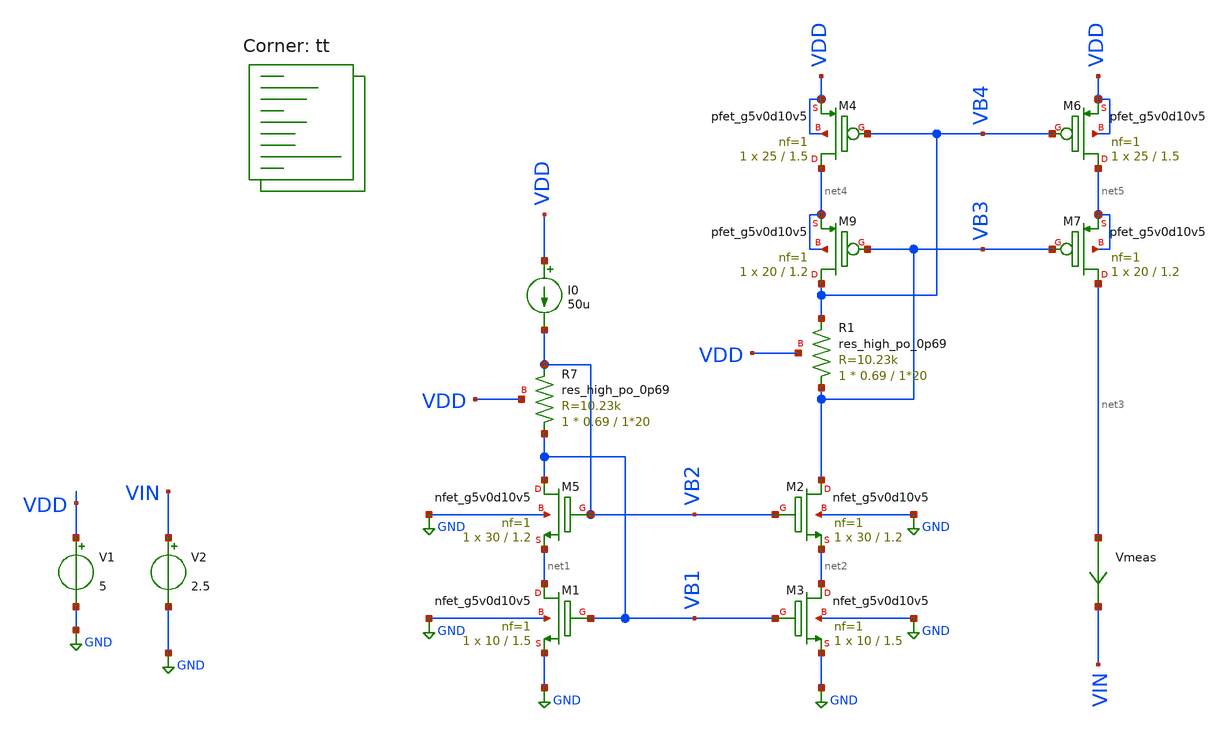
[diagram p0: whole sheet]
** sch_path: folded_cascode_amplifier_upgraded/1_stage/circ_test.sch
**.subckt circ_test
V1 VDD GND 5
V2 VIN GND 2.5
XM5 VB1 VB2 net1 GND sky130_fd_pr__nfet_g5v0d10v5 L=1.2 W=30 nf=1 ad='int((1 + 1)/2) * 30 / 1 * 0.29'
+ as='int((1 + 2)/2) * 30 / 1 * 0.29' pd='2*int((1 + 1)/2) * (30 / 1 + 0.29)' ps='2*int((1 + 2)/2) * (30 / 1 + 0.29)'
+ nrd='0.29 / 30 ' nrs='0.29 / 30 ' sa=0 sb=0 sd=0 mult=1 m=1
XM1 net1 VB1 GND GND sky130_fd_pr__nfet_g5v0d10v5 L=1.5 W=10 nf=1 ad='int((1 + 1)/2) * 10 / 1 * 0.29'
+ as='int((1 + 2)/2) * 10 / 1 * 0.29' pd='2*int((1 + 1)/2) * (10 / 1 + 0.29)' ps='2*int((1 + 2)/2) * (10 / 1 + 0.29)'
+ nrd='0.29 / 10 ' nrs='0.29 / 10 ' sa=0 sb=0 sd=0 mult=1 m=1
XR7 VB1 VB2 VDD sky130_fd_pr__res_high_po_0p69 L=1*20 mult=1 m=1
I0 VDD VB2 50u
XM2 VB3 VB2 net2 GND sky130_fd_pr__nfet_g5v0d10v5 L=1.2 W=30 nf=1 ad='int((1 + 1)/2) * 30 / 1 * 0.29'
+ as='int((1 + 2)/2) * 30 / 1 * 0.29' pd='2*int((1 + 1)/2) * (30 / 1 + 0.29)' ps='2*int((1 + 2)/2) * (30 / 1 + 0.29)'
+ nrd='0.29 / 30 ' nrs='0.29 / 30 ' sa=0 sb=0 sd=0 mult=1 m=1
XM3 net2 VB1 GND GND sky130_fd_pr__nfet_g5v0d10v5 L=1.5 W=10 nf=1 ad='int((1 + 1)/2) * 10 / 1 * 0.29'
+ as='int((1 + 2)/2) * 10 / 1 * 0.29' pd='2*int((1 + 1)/2) * (10 / 1 + 0.29)' ps='2*int((1 + 2)/2) * (10 / 1 + 0.29)'
+ nrd='0.29 / 10 ' nrs='0.29 / 10 ' sa=0 sb=0 sd=0 mult=1 m=1
Vmeas net3 VIN 0
.save i(vmeas)
XR1 VB3 VB4 VDD sky130_fd_pr__res_high_po_0p69 L=1*20 mult=1 m=1
XM9 VB4 VB3 net4 net4 sky130_fd_pr__pfet_g5v0d10v5 L=1.2 W=20 nf=1 ad='int((1 + 1)/2) * 20 / 1 * 0.29'
+ as='int((1 + 2)/2) * 20 / 1 * 0.29' pd='2*int((1 + 1)/2) * (20 / 1 + 0.29)' ps='2*int((1 + 2)/2) * (20 / 1 + 0.29)'
+ nrd='0.29 / 20 ' nrs='0.29 / 20 ' sa=0 sb=0 sd=0 mult=1 m=1
XM4 net4 VB4 VDD VDD sky130_fd_pr__pfet_g5v0d10v5 L=1.5 W=25 nf=1 ad='int((1 + 1)/2) * 25 / 1 * 0.29'
+ as='int((1 + 2)/2) * 25 / 1 * 0.29' pd='2*int((1 + 1)/2) * (25 / 1 + 0.29)' ps='2*int((1 + 2)/2) * (25 / 1 + 0.29)'
+ nrd='0.29 / 25 ' nrs='0.29 / 25 ' sa=0 sb=0 sd=0 mult=1 m=1
XM6 net5 VB4 VDD VDD sky130_fd_pr__pfet_g5v0d10v5 L=1.5 W=25 nf=1 ad='int((1 + 1)/2) * 25 / 1 * 0.29'
+ as='int((1 + 2)/2) * 25 / 1 * 0.29' pd='2*int((1 + 1)/2) * (25 / 1 + 0.29)' ps='2*int((1 + 2)/2) * (25 / 1 + 0.29)'
+ nrd='0.29 / 25 ' nrs='0.29 / 25 ' sa=0 sb=0 sd=0 mult=1 m=1
XM7 net3 VB3 net5 net5 sky130_fd_pr__pfet_g5v0d10v5 L=1.2 W=20 nf=1 ad='int((1 + 1)/2) * 20 / 1 * 0.29'
+ as='int((1 + 2)/2) * 20 / 1 * 0.29' pd='2*int((1 + 1)/2) * (20 / 1 + 0.29)' ps='2*int((1 + 2)/2) * (20 / 1 + 0.29)'
+ nrd='0.29 / 20 ' nrs='0.29 / 20 ' sa=0 sb=0 sd=0 mult=1 m=1
**** begin user architecture code

**************************************************************
**************************************************************
**************************************************************
**************************************************************
**************************************************************
*LIBs*********************************************************
**************************************************************
**************************************************************
**************************************************************
**************************************************************
**************************************************************
*.lib $::SKYWATER_MODELS/sky130.lib.spice tt
* chose the corners in the corner file
* tt_mm for mismatch
* ss ff sf fs standart corners
* ll hh lh hl capacitor and resistors corners
* mc for total process variation including corners
**************************************************************
**************************************************************
**************************************************************
**************************************************************
**************************************************************
*Corners/montecarlo options***********************************
**************************************************************
**************************************************************
**************************************************************
**************************************************************
**************************************************************
.TEMP 27
**************************************************************
**************************************************************
**************************************************************
**************************************************************
*SIMULATION and Plots*****************************************
**************************************************************
**************************************************************
**************************************************************
**************************************************************
.control
save all
dc V2 0 5 0.001
plot i(VMEAS)
plot (1/deriv(i(VMEAS)))
.endc

.lib $::SKYWATER_MODELS/sky130.lib.spice tt
**** end user architecture code
**.ends
.GLOBAL GND
.end
